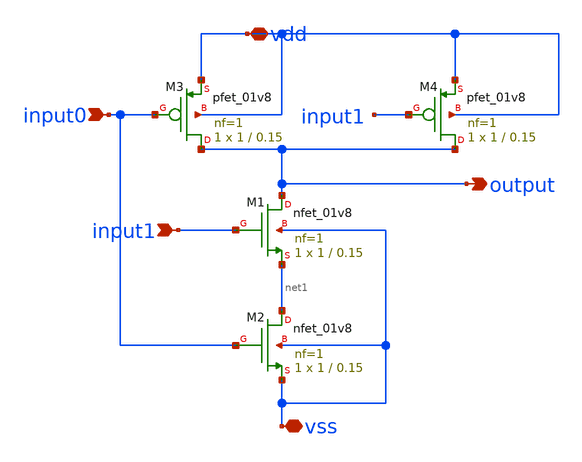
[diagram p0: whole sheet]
** sch_path: xschem/nand.sch
**.subckt nand output input0 vdd input1 vss
*.opin output
*.ipin input0
*.iopin vdd
*.ipin input1
*.iopin vss
XM1 output input1 net1 vss sky130_fd_pr__nfet_01v8 L=0.15 W=1 nf=1 ad='int((nf+1)/2) * W/nf * 0.29' as='int((nf+2)/2) * W/nf * 0.29'
+ pd='2*int((nf+1)/2) * (W/nf + 0.29)' ps='2*int((nf+2)/2) * (W/nf + 0.29)' nrd='0.29 / W' nrs='0.29 / W'
+ sa=0 sb=0 sd=0 mult=1 m=1
XM2 net1 input0 vss vss sky130_fd_pr__nfet_01v8 L=0.15 W=1 nf=1 ad='int((nf+1)/2) * W/nf * 0.29' as='int((nf+2)/2) * W/nf * 0.29'
+ pd='2*int((nf+1)/2) * (W/nf + 0.29)' ps='2*int((nf+2)/2) * (W/nf + 0.29)' nrd='0.29 / W' nrs='0.29 / W'
+ sa=0 sb=0 sd=0 mult=1 m=1
XM3 output input0 vdd vdd sky130_fd_pr__pfet_01v8 L=0.15 W=1 nf=1 ad='int((nf+1)/2) * W/nf * 0.29' as='int((nf+2)/2) * W/nf * 0.29'
+ pd='2*int((nf+1)/2) * (W/nf + 0.29)' ps='2*int((nf+2)/2) * (W/nf + 0.29)' nrd='0.29 / W' nrs='0.29 / W'
+ sa=0 sb=0 sd=0 mult=1 m=1
XM4 output input1 vdd vdd sky130_fd_pr__pfet_01v8 L=0.15 W=1 nf=1 ad='int((nf+1)/2) * W/nf * 0.29' as='int((nf+2)/2) * W/nf * 0.29'
+ pd='2*int((nf+1)/2) * (W/nf + 0.29)' ps='2*int((nf+2)/2) * (W/nf + 0.29)' nrd='0.29 / W' nrs='0.29 / W'
+ sa=0 sb=0 sd=0 mult=1 m=1
**.ends
.end
